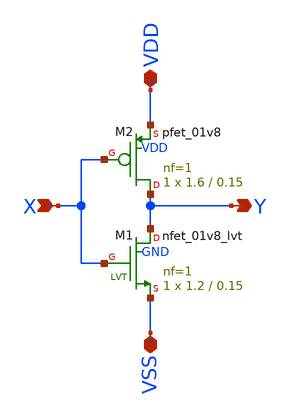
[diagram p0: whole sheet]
** sch_path: schem/inv.sch
**.subckt inv X Y VDD VSS
*.ipin X
*.opin Y
*.iopin VDD
*.iopin VSS
XM1 Y X VSS GND sky130_fd_pr__nfet_01v8_lvt L=0.15 W=1.2 nf=1 ad='int((nf+1)/2) * W/nf * 0.29' as='int((nf+2)/2) * W/nf * 0.29'
+ pd='2*int((nf+1)/2) * (W/nf + 0.29)' ps='2*int((nf+2)/2) * (W/nf + 0.29)' nrd='0.29 / W' nrs='0.29 / W'
+ sa=0 sb=0 sd=0 mult=1 m=1
XM2 Y X VDD VDD sky130_fd_pr__pfet_01v8 L=0.15 W=1.6 nf=1 ad='int((nf+1)/2) * W/nf * 0.29' as='int((nf+2)/2) * W/nf * 0.29'
+ pd='2*int((nf+1)/2) * (W/nf + 0.29)' ps='2*int((nf+2)/2) * (W/nf + 0.29)' nrd='0.29 / W' nrs='0.29 / W'
+ sa=0 sb=0 sd=0 mult=1 m=1
**.ends
.end
